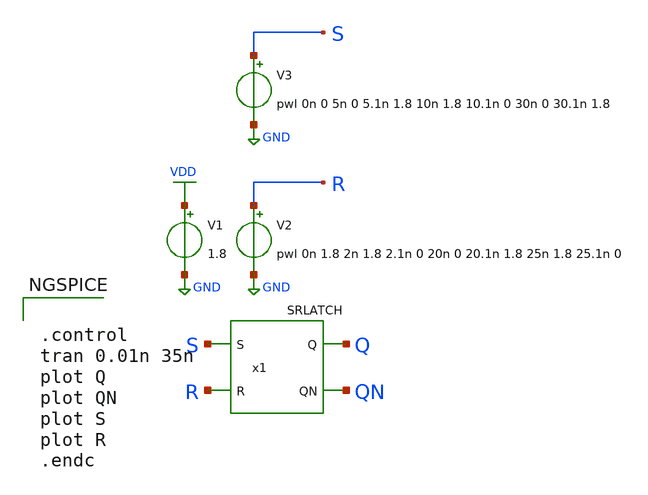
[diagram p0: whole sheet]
** sch_path: archives/lib/xschem/test_SRLATCH.sch
**.subckt test_SRLATCH
V2 R GND pwl 0n 1.8 2n 1.8 2.1n 0 20n 0 20.1n 1.8 25n 1.8 25.1n 0
V1 VDD GND 1.8
V3 S GND pwl 0n 0 5n 0 5.1n 1.8 10n 1.8 10.1n 0 30n 0 30.1n 1.8
x1 Q QN S R VDD GND SRLATCH
**** begin user architecture code

.lib $::SKYWATER_MODELS/sky130.lib.spice tt


**** end user architecture code
**.ends
.GLOBAL VDD
.GLOBAL GND
**** begin user architecture code


.control
tran 0.01n 35n
plot Q
plot QN
plot S
plot R
.endc


**** end user architecture code
.end
